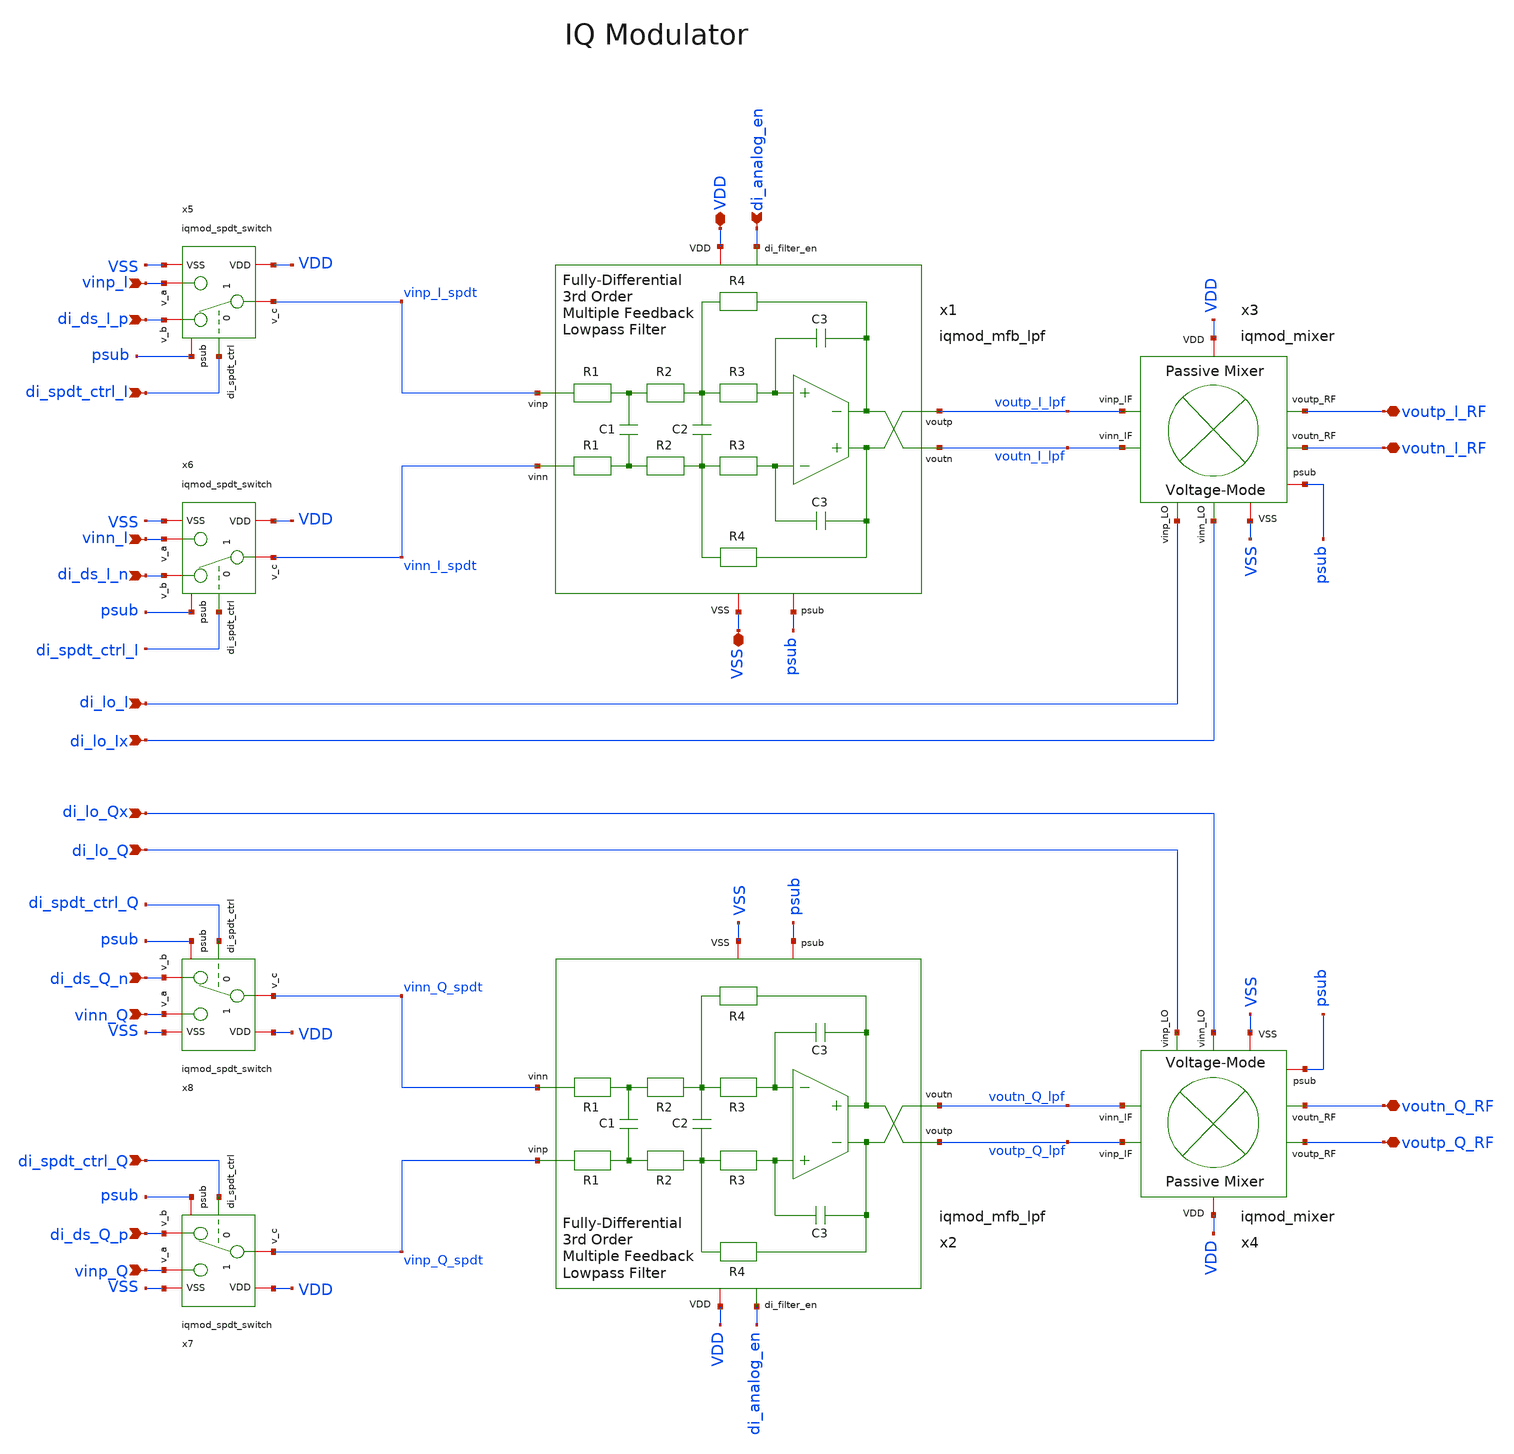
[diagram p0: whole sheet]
** sch_path: ihp130/macros/iqmod/xschem/iqmod_top.sch
**.subckt iqmod_top VDD voutp_I_RF VSS di_lo_Q di_lo_Qx di_lo_I di_lo_Ix di_ds_I_p voutn_I_RF
*+ voutp_Q_RF voutn_Q_RF di_analog_en vinp_I vinn_I di_spdt_ctrl_I di_ds_I_n di_ds_Q_p vinp_Q vinn_Q
*+ di_spdt_ctrl_Q di_ds_Q_n
*.iopin VDD
*.iopin voutp_I_RF
*.iopin VSS
*.ipin di_lo_Q
*.ipin di_lo_Qx
*.ipin di_lo_I
*.ipin di_lo_Ix
*.ipin di_ds_I_p
*.iopin voutn_I_RF
*.iopin voutp_Q_RF
*.iopin voutn_Q_RF
*.ipin di_analog_en
*.ipin vinp_I
*.ipin vinn_I
*.ipin di_spdt_ctrl_I
*.ipin di_ds_I_n
*.ipin di_ds_Q_p
*.ipin vinp_Q
*.ipin vinn_Q
*.ipin di_spdt_ctrl_Q
*.ipin di_ds_Q_n
x3 voutp_I_lpf voutn_I_lpf voutp_I_RF di_lo_I di_lo_Ix VDD VSS voutn_I_RF psub iqmod_mixer
x4 voutp_Q_lpf voutn_Q_lpf voutp_Q_RF di_lo_Q di_lo_Qx VDD VSS voutn_Q_RF psub iqmod_mixer
x1 voutp_I_lpf vinp_I_spdt voutn_I_lpf vinn_I_spdt VDD VSS di_analog_en psub iqmod_mfb_lpf
x2 voutp_Q_lpf vinp_Q_spdt voutn_Q_lpf vinn_Q_spdt VDD VSS di_analog_en psub iqmod_mfb_lpf
x5 VDD di_spdt_ctrl_I VSS vinp_I_spdt di_ds_I_p vinp_I psub iqmod_spdt_switch
x6 VDD di_spdt_ctrl_I VSS vinn_I_spdt di_ds_I_n vinn_I psub iqmod_spdt_switch
x7 VDD di_spdt_ctrl_Q VSS vinp_Q_spdt di_ds_Q_p vinp_Q psub iqmod_spdt_switch
x8 VDD di_spdt_ctrl_Q VSS vinn_Q_spdt di_ds_Q_n vinn_Q psub iqmod_spdt_switch
**.ends
.end
